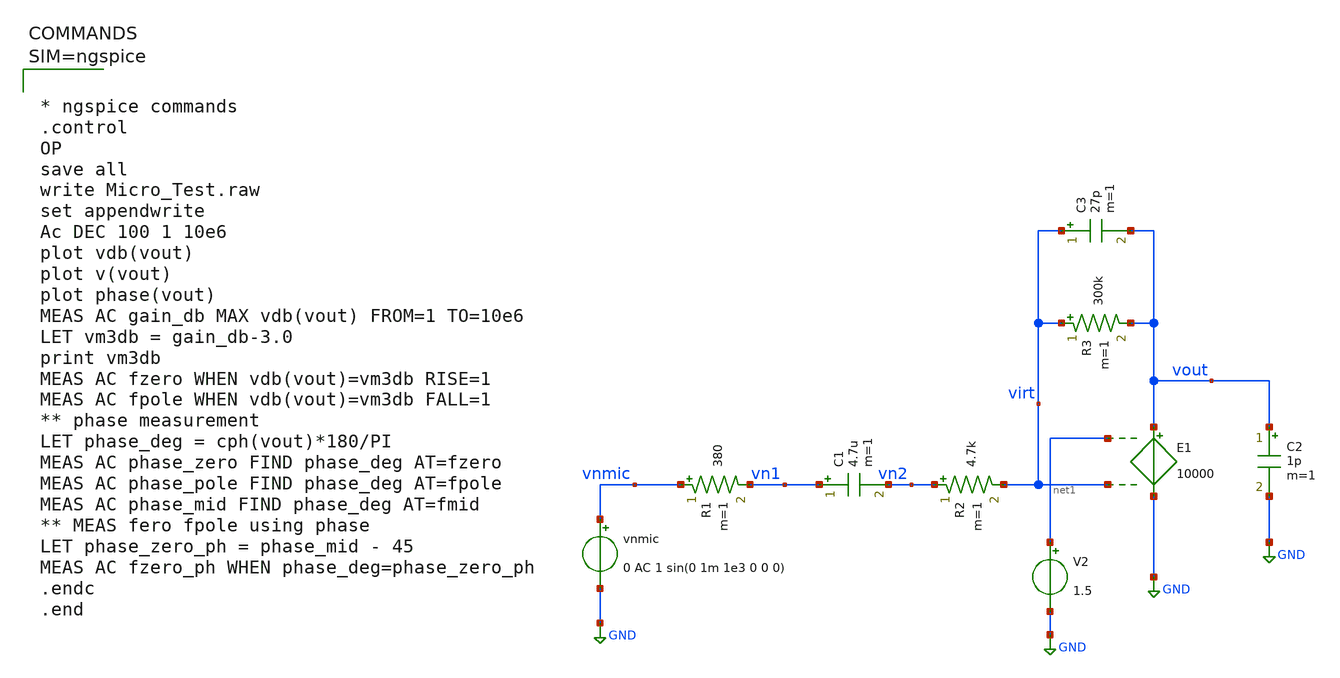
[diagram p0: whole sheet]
** sch_path: xschem/Micro_Test.sch
**.subckt Micro_Test
vnmic vnmic GND 0 AC 1 sin(0 1m 1e3 0 0 0)
R1 vnmic vn1 380 m=1
C1 vn1 vn2 4.7u m=1
R2 vn2 virt 4.7k m=1
E1 vout GND net1 virt 10000
V2 net1 GND 1.5
C2 vout GND 1p m=1
R3 virt vout 300k m=1
C3 virt vout 27p m=1
**** begin user architecture code



* ngspice commands
.control
OP
save all
write Micro_Test.raw
set appendwrite
Ac DEC 100 1 10e6
plot vdb(vout)
plot v(vout)
plot phase(vout)
MEAS AC gain_db MAX vdb(vout) FROM=1 TO=10e6
LET vm3db = gain_db-3.0
print vm3db
MEAS AC fzero WHEN vdb(vout)=vm3db RISE=1
MEAS AC fpole WHEN vdb(vout)=vm3db FALL=1
** phase measurement
LET phase_deg = cph(vout)*180/PI
MEAS AC phase_zero FIND phase_deg AT=fzero
MEAS AC phase_pole FIND phase_deg AT=fpole
MEAS AC phase_mid FIND phase_deg AT=fmid
** MEAS fero fpole using phase
LET phase_zero_ph = phase_mid - 45
MEAS AC fzero_ph WHEN phase_deg=phase_zero_ph
.endc
.end



**** end user architecture code
**.ends
.GLOBAL GND
.end
